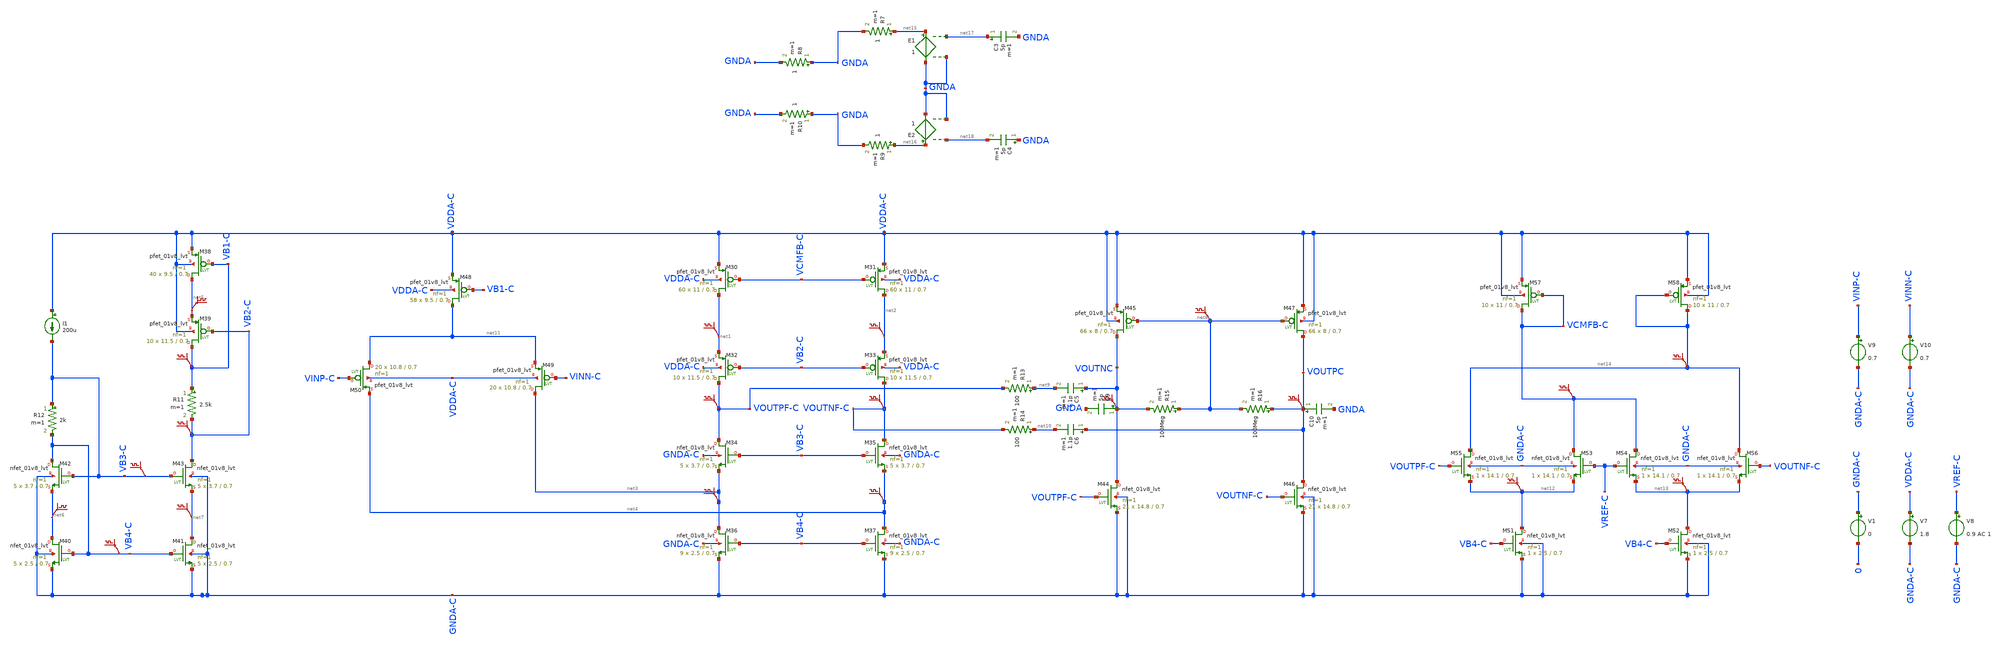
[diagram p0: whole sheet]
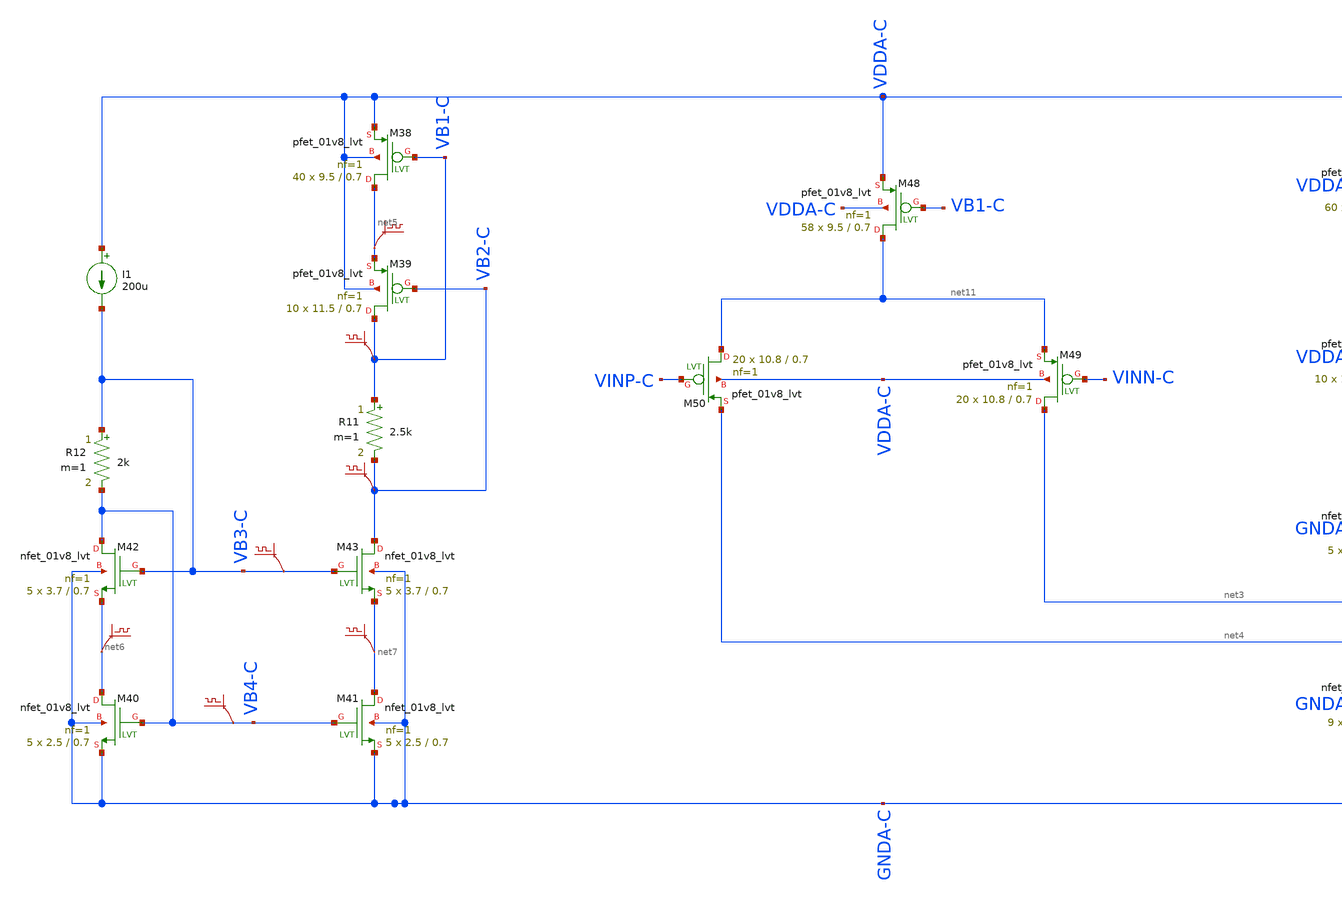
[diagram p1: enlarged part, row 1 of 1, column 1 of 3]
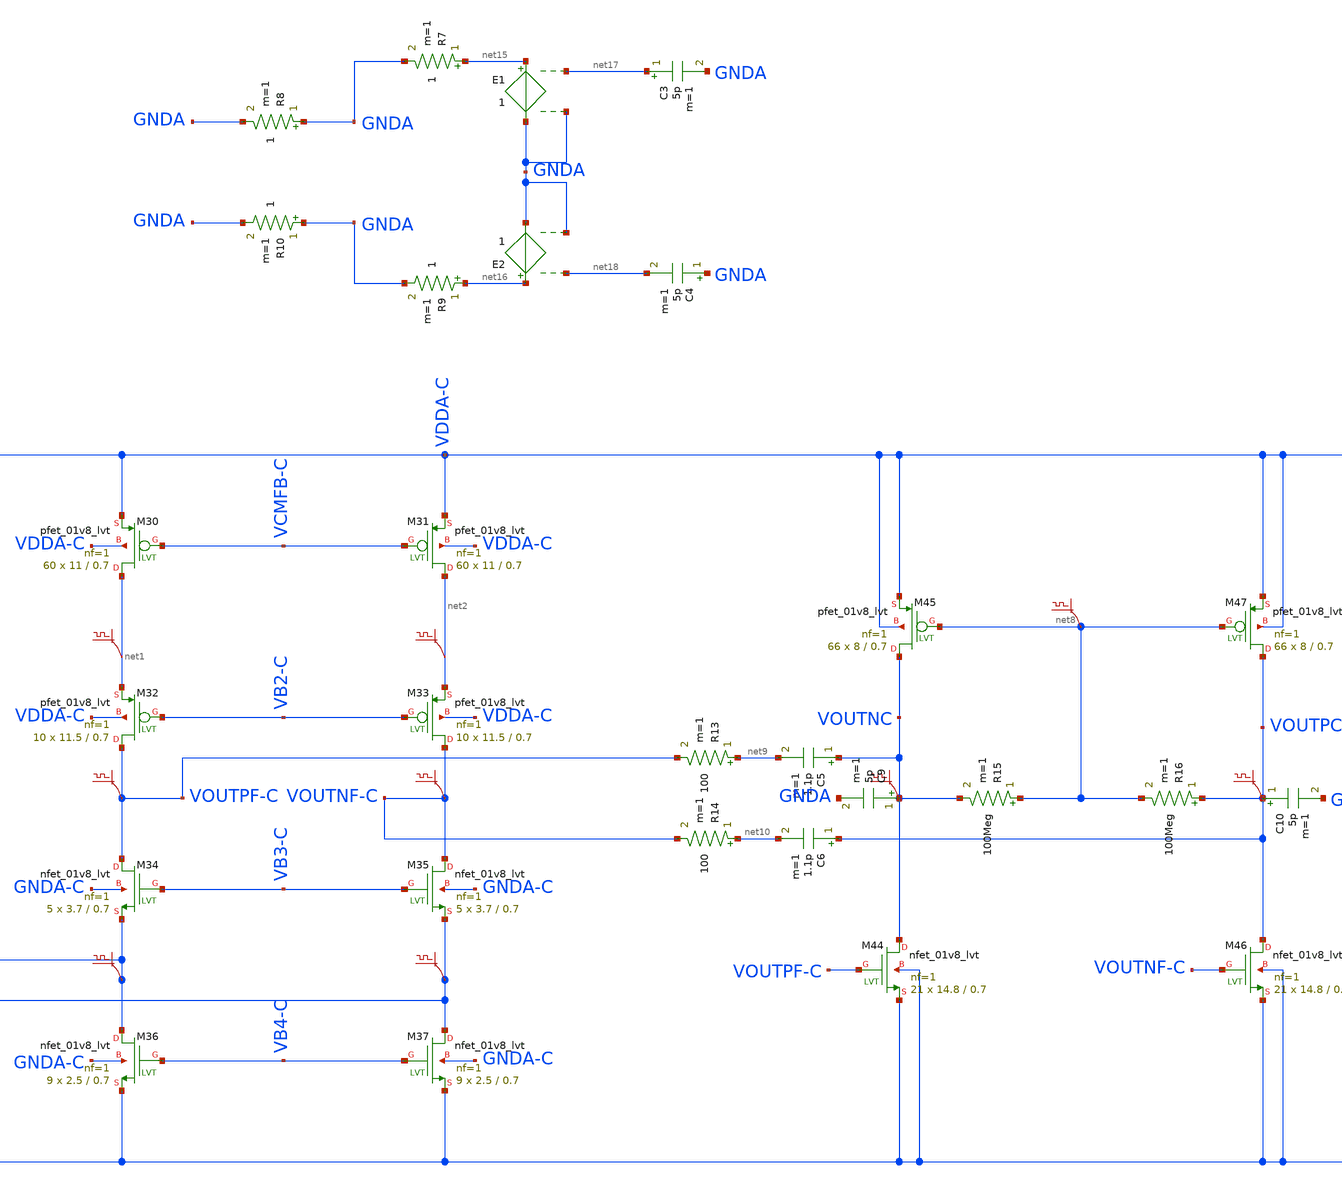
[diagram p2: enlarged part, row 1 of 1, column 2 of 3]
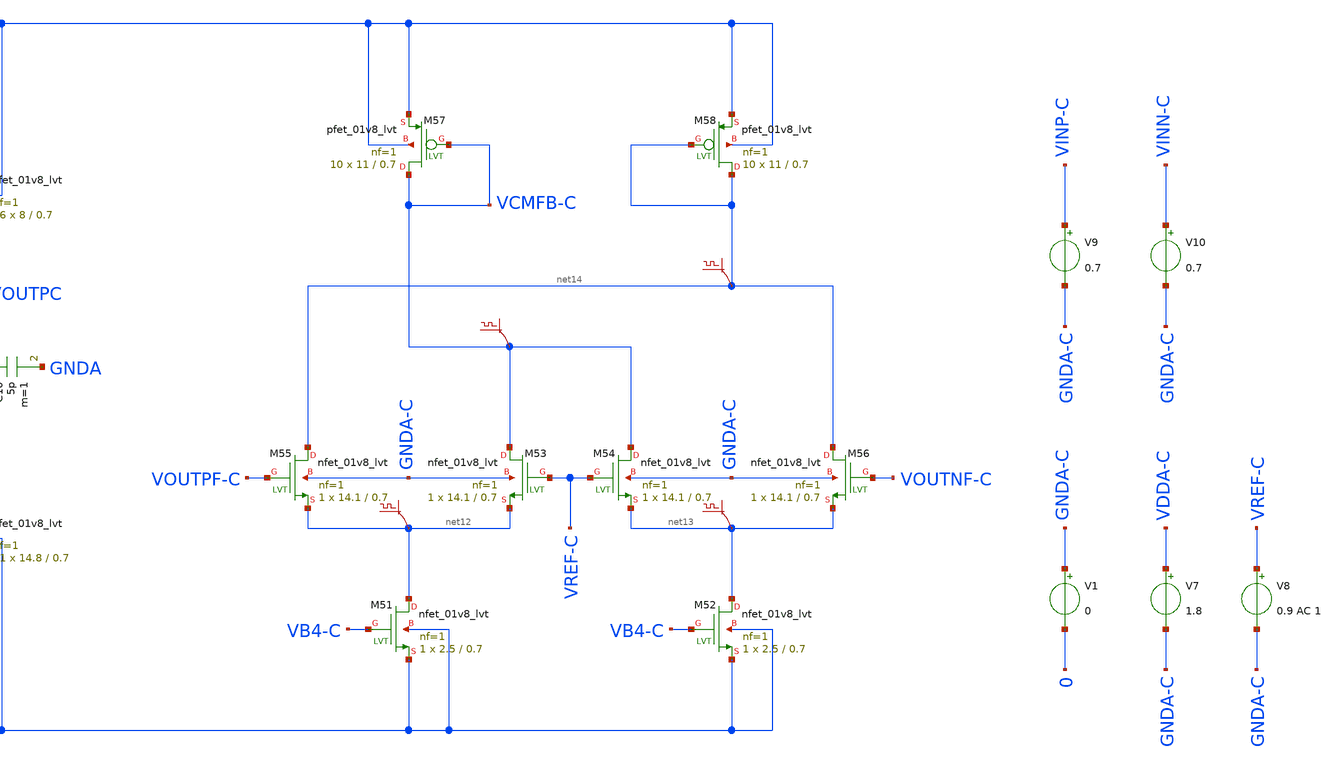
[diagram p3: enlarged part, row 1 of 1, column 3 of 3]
** sch_path: untitled.sch
**.subckt untitled
XM30 net1 VCMFB-C VDDA-C VDDA-C sky130_fd_pr__pfet_01v8_lvt L=0.7 W=11 nf=1 ad='int((nf+1)/2) * W/nf * 0.29'
+ as='int((nf+2)/2) * W/nf * 0.29' pd='2*int((nf+1)/2) * (W/nf + 0.29)' ps='2*int((nf+2)/2) * (W/nf + 0.29)'
+ nrd='0.29 / W' nrs='0.29 / W' sa=0 sb=0 sd=0 mult=60 m=60
XM31 net2 VCMFB-C VDDA-C VDDA-C sky130_fd_pr__pfet_01v8_lvt L=0.7 W=11 nf=1 ad='int((nf+1)/2) * W/nf * 0.29'
+ as='int((nf+2)/2) * W/nf * 0.29' pd='2*int((nf+1)/2) * (W/nf + 0.29)' ps='2*int((nf+2)/2) * (W/nf + 0.29)'
+ nrd='0.29 / W' nrs='0.29 / W' sa=0 sb=0 sd=0 mult=60 m=60
XM32 VOUTPF-C VB2-C net1 VDDA-C sky130_fd_pr__pfet_01v8_lvt L=0.7 W=11.5 nf=1 ad='int((nf+1)/2) * W/nf * 0.29'
+ as='int((nf+2)/2) * W/nf * 0.29' pd='2*int((nf+1)/2) * (W/nf + 0.29)' ps='2*int((nf+2)/2) * (W/nf + 0.29)'
+ nrd='0.29 / W' nrs='0.29 / W' sa=0 sb=0 sd=0 mult=10 m=10
XM33 VOUTNF-C VB2-C net2 VDDA-C sky130_fd_pr__pfet_01v8_lvt L=0.7 W=11.5 nf=1 ad='int((nf+1)/2) * W/nf * 0.29'
+ as='int((nf+2)/2) * W/nf * 0.29' pd='2*int((nf+1)/2) * (W/nf + 0.29)' ps='2*int((nf+2)/2) * (W/nf + 0.29)'
+ nrd='0.29 / W' nrs='0.29 / W' sa=0 sb=0 sd=0 mult=10 m=10
XM34 VOUTPF-C VB3-C net3 GNDA-C sky130_fd_pr__nfet_01v8_lvt L=0.7 W=3.7 nf=1 ad='int((nf+1)/2) * W/nf * 0.29'
+ as='int((nf+2)/2) * W/nf * 0.29' pd='2*int((nf+1)/2) * (W/nf + 0.29)' ps='2*int((nf+2)/2) * (W/nf + 0.29)'
+ nrd='0.29 / W' nrs='0.29 / W' sa=0 sb=0 sd=0 mult=5 m=5
XM35 VOUTNF-C VB3-C net4 GNDA-C sky130_fd_pr__nfet_01v8_lvt L=0.7 W=3.7 nf=1 ad='int((nf+1)/2) * W/nf * 0.29'
+ as='int((nf+2)/2) * W/nf * 0.29' pd='2*int((nf+1)/2) * (W/nf + 0.29)' ps='2*int((nf+2)/2) * (W/nf + 0.29)'
+ nrd='0.29 / W' nrs='0.29 / W' sa=0 sb=0 sd=0 mult=5 m=5
XM36 net3 VB4-C GNDA-C GNDA-C sky130_fd_pr__nfet_01v8_lvt L=0.7 W=2.5 nf=1 ad='int((nf+1)/2) * W/nf * 0.29'
+ as='int((nf+2)/2) * W/nf * 0.29' pd='2*int((nf+1)/2) * (W/nf + 0.29)' ps='2*int((nf+2)/2) * (W/nf + 0.29)'
+ nrd='0.29 / W' nrs='0.29 / W' sa=0 sb=0 sd=0 mult=9 m=9
XM37 net4 VB4-C GNDA-C GNDA-C sky130_fd_pr__nfet_01v8_lvt L=0.7 W=2.5 nf=1 ad='int((nf+1)/2) * W/nf * 0.29'
+ as='int((nf+2)/2) * W/nf * 0.29' pd='2*int((nf+1)/2) * (W/nf + 0.29)' ps='2*int((nf+2)/2) * (W/nf + 0.29)'
+ nrd='0.29 / W' nrs='0.29 / W' sa=0 sb=0 sd=0 mult=9 m=9
XM38 net5 VB1-C VDDA-C VDDA-C sky130_fd_pr__pfet_01v8_lvt L=0.7 W=9.5 nf=1 ad='int((nf+1)/2) * W/nf * 0.29'
+ as='int((nf+2)/2) * W/nf * 0.29' pd='2*int((nf+1)/2) * (W/nf + 0.29)' ps='2*int((nf+2)/2) * (W/nf + 0.29)'
+ nrd='0.29 / W' nrs='0.29 / W' sa=0 sb=0 sd=0 mult=40 m=40
XM39 VB1-C VB2-C net5 VDDA-C sky130_fd_pr__pfet_01v8_lvt L=0.7 W=11.5 nf=1 ad='int((nf+1)/2) * W/nf * 0.29'
+ as='int((nf+2)/2) * W/nf * 0.29' pd='2*int((nf+1)/2) * (W/nf + 0.29)' ps='2*int((nf+2)/2) * (W/nf + 0.29)'
+ nrd='0.29 / W' nrs='0.29 / W' sa=0 sb=0 sd=0 mult=10 m=10
.save v(vb1-c)
.save v(net5)
R11 VB1-C VB2-C 2.5k m=1
.save v(vb2-c)
XM40 net6 VB4-C GNDA-C GNDA-C sky130_fd_pr__nfet_01v8_lvt L=0.7 W=2.5 nf=1 ad='int((nf+1)/2) * W/nf * 0.29'
+ as='int((nf+2)/2) * W/nf * 0.29' pd='2*int((nf+1)/2) * (W/nf + 0.29)' ps='2*int((nf+2)/2) * (W/nf + 0.29)'
+ nrd='0.29 / W' nrs='0.29 / W' sa=0 sb=0 sd=0 mult=5 m=5
XM41 net7 VB4-C GNDA-C GNDA-C sky130_fd_pr__nfet_01v8_lvt L=0.7 W=2.5 nf=1 ad='int((nf+1)/2) * W/nf * 0.29'
+ as='int((nf+2)/2) * W/nf * 0.29' pd='2*int((nf+1)/2) * (W/nf + 0.29)' ps='2*int((nf+2)/2) * (W/nf + 0.29)'
+ nrd='0.29 / W' nrs='0.29 / W' sa=0 sb=0 sd=0 mult=5 m=5
XM42 VB4-C VB3-C net6 GNDA-C sky130_fd_pr__nfet_01v8_lvt L=0.7 W=3.7 nf=1 ad='int((nf+1)/2) * W/nf * 0.29'
+ as='int((nf+2)/2) * W/nf * 0.29' pd='2*int((nf+1)/2) * (W/nf + 0.29)' ps='2*int((nf+2)/2) * (W/nf + 0.29)'
+ nrd='0.29 / W' nrs='0.29 / W' sa=0 sb=0 sd=0 mult=5 m=5
XM43 VB2-C VB3-C net7 GNDA-C sky130_fd_pr__nfet_01v8_lvt L=0.7 W=3.7 nf=1 ad='int((nf+1)/2) * W/nf * 0.29'
+ as='int((nf+2)/2) * W/nf * 0.29' pd='2*int((nf+1)/2) * (W/nf + 0.29)' ps='2*int((nf+2)/2) * (W/nf + 0.29)'
+ nrd='0.29 / W' nrs='0.29 / W' sa=0 sb=0 sd=0 mult=5 m=5
.save v(net6)
.save v(net7)
.save v(vb4-c)
R12 VB3-C VB4-C 2k m=1
I1 VDDA-C VB3-C 200u
XM44 VOUTNC VOUTPF-C GNDA-C GNDA-C sky130_fd_pr__nfet_01v8_lvt L=0.7 W=14.8 nf=1 ad='int((nf+1)/2) * W/nf * 0.29'
+ as='int((nf+2)/2) * W/nf * 0.29' pd='2*int((nf+1)/2) * (W/nf + 0.29)' ps='2*int((nf+2)/2) * (W/nf + 0.29)'
+ nrd='0.29 / W' nrs='0.29 / W' sa=0 sb=0 sd=0 mult=21 m=21
XM45 VOUTNC net8 VDDA-C VDDA-C sky130_fd_pr__pfet_01v8_lvt L=0.7 W=8 nf=1 ad='int((nf+1)/2) * W/nf * 0.29'
+ as='int((nf+2)/2) * W/nf * 0.29' pd='2*int((nf+1)/2) * (W/nf + 0.29)' ps='2*int((nf+2)/2) * (W/nf + 0.29)'
+ nrd='0.29 / W' nrs='0.29 / W' sa=0 sb=0 sd=0 mult=66 m=66
XM46 VOUTPC VOUTNF-C GNDA-C GNDA-C sky130_fd_pr__nfet_01v8_lvt L=0.7 W=14.8 nf=1 ad='int((nf+1)/2) * W/nf * 0.29'
+ as='int((nf+2)/2) * W/nf * 0.29' pd='2*int((nf+1)/2) * (W/nf + 0.29)' ps='2*int((nf+2)/2) * (W/nf + 0.29)'
+ nrd='0.29 / W' nrs='0.29 / W' sa=0 sb=0 sd=0 mult=21 m=21
XM47 VOUTPC net8 VDDA-C VDDA-C sky130_fd_pr__pfet_01v8_lvt L=0.7 W=8 nf=1 ad='int((nf+1)/2) * W/nf * 0.29'
+ as='int((nf+2)/2) * W/nf * 0.29' pd='2*int((nf+1)/2) * (W/nf + 0.29)' ps='2*int((nf+2)/2) * (W/nf + 0.29)'
+ nrd='0.29 / W' nrs='0.29 / W' sa=0 sb=0 sd=0 mult=66 m=66
R13 net9 VOUTPF-C 100 m=1
R14 net10 VOUTNF-C 100 m=1
C5 VOUTNC net9 1.1p m=1
C6 VOUTPC net10 1.1p m=1
.save v(net1)
.save v(net2)
.save v(voutpf-c)
.save v(voutnf-c)
.save v(net3)
.save v(net4)
.save v(voutnc)
.save v(voutpc)
.save v(vb3-c)
XM48 net11 VB1-C VDDA-C VDDA-C sky130_fd_pr__pfet_01v8_lvt L=0.7 W=9.5 nf=1 ad='int((nf+1)/2) * W/nf * 0.29'
+ as='int((nf+2)/2) * W/nf * 0.29' pd='2*int((nf+1)/2) * (W/nf + 0.29)' ps='2*int((nf+2)/2) * (W/nf + 0.29)'
+ nrd='0.29 / W' nrs='0.29 / W' sa=0 sb=0 sd=0 mult=58 m=58
XM49 net3 VINN-C net11 VDDA-C sky130_fd_pr__pfet_01v8_lvt L=0.7 W=10.8 nf=1 ad='int((nf+1)/2) * W/nf * 0.29'
+ as='int((nf+2)/2) * W/nf * 0.29' pd='2*int((nf+1)/2) * (W/nf + 0.29)' ps='2*int((nf+2)/2) * (W/nf + 0.29)'
+ nrd='0.29 / W' nrs='0.29 / W' sa=0 sb=0 sd=0 mult=20 m=20
XM50 net11 VINP-C net4 VDDA-C sky130_fd_pr__pfet_01v8_lvt L=0.7 W=10.8 nf=1 ad='int((nf+1)/2) * W/nf * 0.29'
+ as='int((nf+2)/2) * W/nf * 0.29' pd='2*int((nf+1)/2) * (W/nf + 0.29)' ps='2*int((nf+2)/2) * (W/nf + 0.29)'
+ nrd='0.29 / W' nrs='0.29 / W' sa=0 sb=0 sd=0 mult=20 m=20
R15 net8 VOUTNC 100Meg m=1
R16 VOUTPC net8 100Meg m=1
XM51 net12 VB4-C GNDA-C GNDA-C sky130_fd_pr__nfet_01v8_lvt L=0.7 W=2.5 nf=1 ad='int((nf+1)/2) * W/nf * 0.29'
+ as='int((nf+2)/2) * W/nf * 0.29' pd='2*int((nf+1)/2) * (W/nf + 0.29)' ps='2*int((nf+2)/2) * (W/nf + 0.29)'
+ nrd='0.29 / W' nrs='0.29 / W' sa=0 sb=0 sd=0 mult=1 m=1
XM52 net13 VB4-C GNDA-C GNDA-C sky130_fd_pr__nfet_01v8_lvt L=0.7 W=2.5 nf=1 ad='int((nf+1)/2) * W/nf * 0.29'
+ as='int((nf+2)/2) * W/nf * 0.29' pd='2*int((nf+1)/2) * (W/nf + 0.29)' ps='2*int((nf+2)/2) * (W/nf + 0.29)'
+ nrd='0.29 / W' nrs='0.29 / W' sa=0 sb=0 sd=0 mult=1 m=1
XM53 VCMFB-C VREF-C net12 GNDA-C sky130_fd_pr__nfet_01v8_lvt L=0.7 W=14.1 nf=1 ad='int((nf+1)/2) * W/nf * 0.29'
+ as='int((nf+2)/2) * W/nf * 0.29' pd='2*int((nf+1)/2) * (W/nf + 0.29)' ps='2*int((nf+2)/2) * (W/nf + 0.29)'
+ nrd='0.29 / W' nrs='0.29 / W' sa=0 sb=0 sd=0 mult=1 m=1
XM54 VCMFB-C VREF-C net13 GNDA-C sky130_fd_pr__nfet_01v8_lvt L=0.7 W=14.1 nf=1 ad='int((nf+1)/2) * W/nf * 0.29'
+ as='int((nf+2)/2) * W/nf * 0.29' pd='2*int((nf+1)/2) * (W/nf + 0.29)' ps='2*int((nf+2)/2) * (W/nf + 0.29)'
+ nrd='0.29 / W' nrs='0.29 / W' sa=0 sb=0 sd=0 mult=1 m=1
XM55 net14 VOUTPF-C net12 GNDA-C sky130_fd_pr__nfet_01v8_lvt L=0.7 W=14.1 nf=1 ad='int((nf+1)/2) * W/nf * 0.29'
+ as='int((nf+2)/2) * W/nf * 0.29' pd='2*int((nf+1)/2) * (W/nf + 0.29)' ps='2*int((nf+2)/2) * (W/nf + 0.29)'
+ nrd='0.29 / W' nrs='0.29 / W' sa=0 sb=0 sd=0 mult=1 m=1
XM56 net14 VOUTNF-C net13 GNDA-C sky130_fd_pr__nfet_01v8_lvt L=0.7 W=14.1 nf=1 ad='int((nf+1)/2) * W/nf * 0.29'
+ as='int((nf+2)/2) * W/nf * 0.29' pd='2*int((nf+1)/2) * (W/nf + 0.29)' ps='2*int((nf+2)/2) * (W/nf + 0.29)'
+ nrd='0.29 / W' nrs='0.29 / W' sa=0 sb=0 sd=0 mult=1 m=1
XM57 VCMFB-C VCMFB-C VDDA-C VDDA-C sky130_fd_pr__pfet_01v8_lvt L=0.7 W=11 nf=1 ad='int((nf+1)/2) * W/nf * 0.29'
+ as='int((nf+2)/2) * W/nf * 0.29' pd='2*int((nf+1)/2) * (W/nf + 0.29)' ps='2*int((nf+2)/2) * (W/nf + 0.29)'
+ nrd='0.29 / W' nrs='0.29 / W' sa=0 sb=0 sd=0 mult=10 m=10
XM58 net14 net14 VDDA-C VDDA-C sky130_fd_pr__pfet_01v8_lvt L=0.7 W=11 nf=1 ad='int((nf+1)/2) * W/nf * 0.29'
+ as='int((nf+2)/2) * W/nf * 0.29' pd='2*int((nf+1)/2) * (W/nf + 0.29)' ps='2*int((nf+2)/2) * (W/nf + 0.29)'
+ nrd='0.29 / W' nrs='0.29 / W' sa=0 sb=0 sd=0 mult=10 m=10
.save v(net12)
.save v(net13)
.save v(vcmfb-c)
.save v(net14)
.save v(net8)
V1 GNDA-C 0 0
V7 VDDA-C GNDA-C 1.8
V8 VREF-C GNDA-C 0.9 AC 1
V9 VINP-C GNDA-C 0.7
V10 VINN-C GNDA-C 0.7
C9 VOUTNC GNDA 5p m=1
C10 VOUTPC GNDA 5p m=1
C3 net17 GNDA 5p m=1
C4 GNDA net18 5p m=1
R7 net15 GNDA 1 m=1
R8 GNDA GNDA 1 m=1
R9 net16 GNDA 1 m=1
R10 GNDA GNDA 1 m=1
E1 net15 GNDA net17 GNDA 1
E2 net16 GNDA net18 GNDA 1
**.ends
.end
